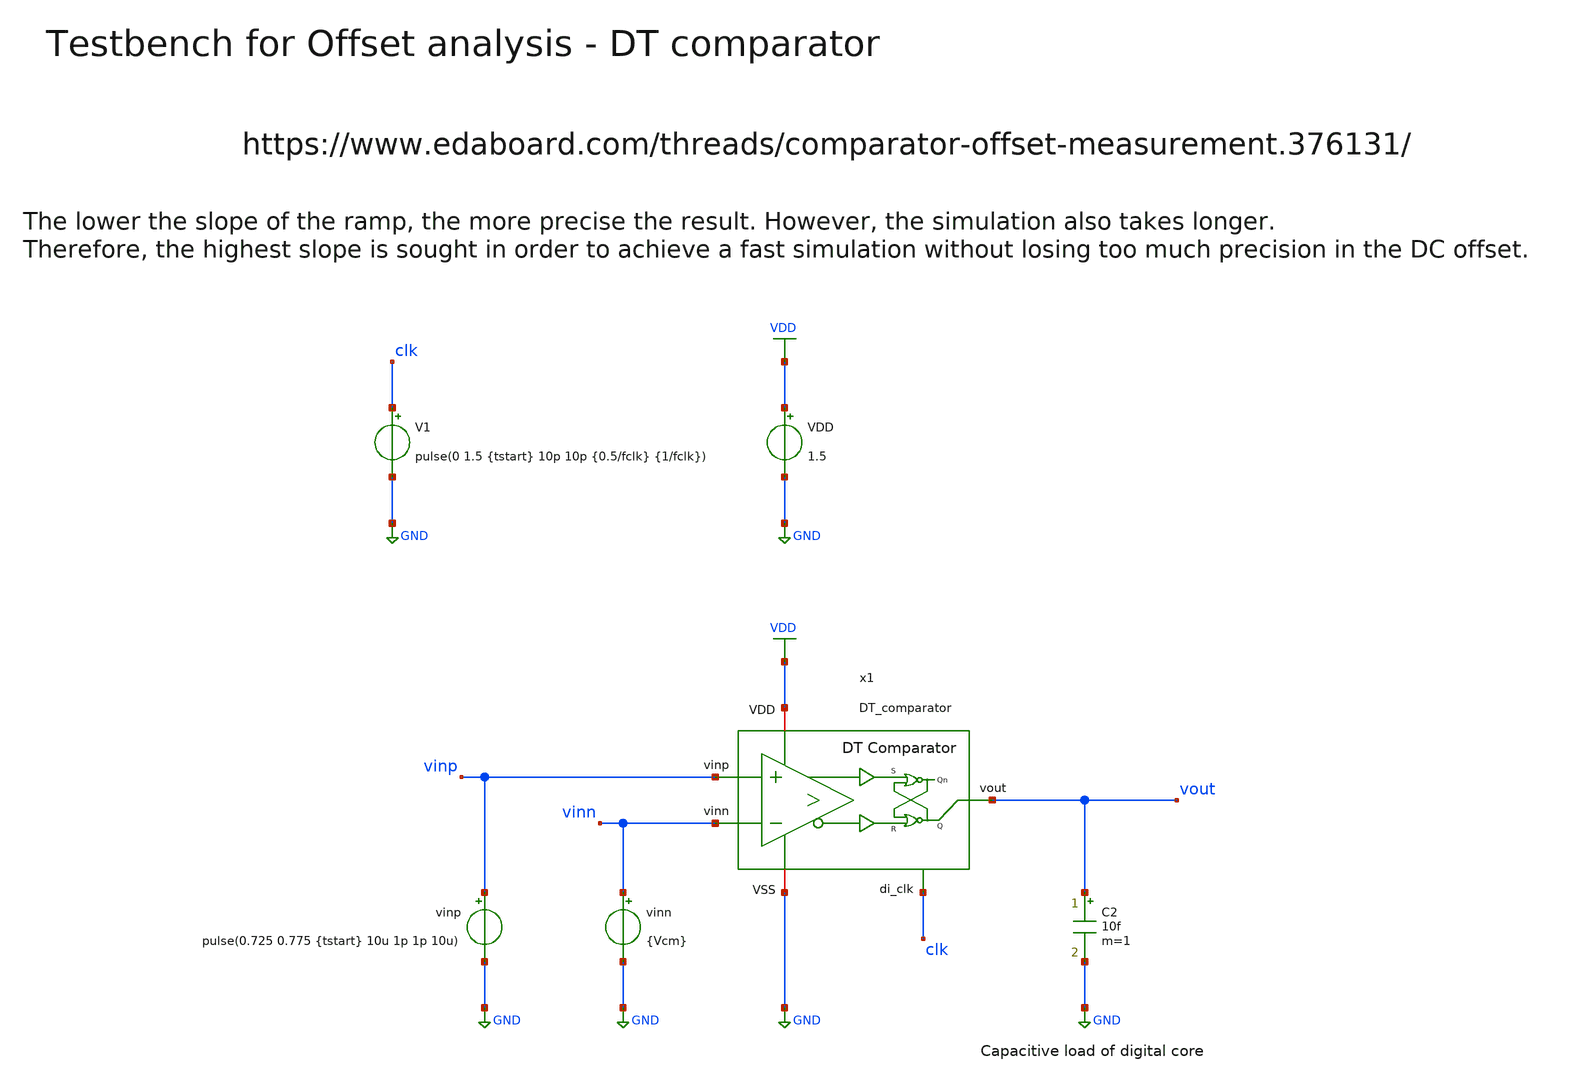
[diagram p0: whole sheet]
** sch_path: SG13G2_ATBS-ADC-main/xschem/comparator/discrete_time/testbenches/DT_comparator_tb_tran_offset.sch
**.subckt DT_comparator_tb_tran_offset
VDD VDD GND 1.5
V1 clk GND pulse(0 1.5 {tstart} 10p 10p {0.5/fclk} {1/fclk})
vinp vinp GND pulse(0.725 0.775 {tstart} 10u 1p 1p 10u)
vinn vinn GND {Vcm}
C2 vout GND 10f m=1
x1 VDD vinp vout vinn clk GND DT_comparator
**** begin user architecture code

.lib cornerMOSlv.lib mos_tt
.lib cornerMOShv.lib mos_tt
.lib cornerRES.lib res_typ



.param temp=27
.param fclk=8000000
.param tstart=2n
.param Vcm=0.75
.csparam fclk=fclk
.csparam tstart=tstart
.csparam Vcm=Vcm
.options klu method=gear reltol=1e-5 abstol=1e-12 gmin=1e-15
.ic v(vout) = 0
.control
* save all

* User Constants
let tstop = 10u
let tstep = 1/fclk

* Operating Point Analysis
op
remzerovec
write DT_comparator_tb_tran_offset.raw
set appendwrite

* Transient Analysis
tran $&tstep $&tstop
write DT_comparator_tb_tran_offset.raw

* Measure offset
let vout_limit = 0.9 * 1.5
meas tran tcross WHEN v(vout)=vout_limit CROSS=1
print tcross
meas tran vinp_voff FIND v(vinp) at=tcross CROSS=1
let voff = vinp_voff - Vcm
print voff

* Plotting
plot v(clk) v(vout) v(vinp) v(vinn)

* Writing Data
set wr_singlescale
set wr_vecnames
wrdata
+ /foss/designs/SG13G2_ATBS-ADC-main/python/plot_simulations/data/DT_comparator_tb_tran_offset.txt v(clk) v(vout) v(vinp) v(vinn)


*quit
.endc

**** end user architecture code
**.ends

* expanding   symbol:  comparator/discrete_time/DT_comparator.sym # of pins=6
** sym_path: SG13G2_ATBS-ADC-main/xschem/comparator/discrete_time/DT_comparator.sym
** sch_path: SG13G2_ATBS-ADC-main/xschem/comparator/discrete_time/DT_comparator.sch
.subckt DT_comparator VDD vinp vout vinn di_clk VSS
*.iopin VDD
*.opin vout
*.iopin VSS
*.ipin vinp
*.ipin vinn
*.ipin di_clk
x2 VDD voutp_comp voutp_buf VSS buffer_lv W_P_INV=1.0u L_P_INV=0.13u W_N_INV=1.0u L_N_INV=0.13u
x3 VDD voutn_comp voutn_buf VSS buffer_lv W_P_INV=1.0u L_P_INV=0.13u W_N_INV=1.0u L_N_INV=0.13u
x5 VDD di_clk net1 VSS inverter_lv W_P=1.0u L_P=0.13u W_N=1.0u L_N=0.13u
* noconn #net2
x4 VDD voutp_buf net2 VSS vout voutn_buf SR_latch W_P_SR=1.0u L_P_SR=0.13u W_N_SR=1.0u L_N_SR=0.13u
x1 net1 di_clk VDD voutp_comp vinp VSS voutn_comp vinn dynamic_biasing_comparator
.ends


* expanding   symbol:  buffer/buffer_lv.sym # of pins=4
** sym_path: SG13G2_ATBS-ADC-main/xschem/buffer/buffer_lv.sym
** sch_path: SG13G2_ATBS-ADC-main/xschem/buffer/buffer_lv.sch
.subckt buffer_lv VDD vin vout VSS  W_P_INV=3.0u L_P_INV=0.13u W_N_INV=1.0u L_N_INV=0.13u
*.ipin vin
*.iopin VDD
*.iopin VSS
*.opin vout
x1 VDD vin net1 VSS inverter_lv W_P=W_P_INV L_P=L_P_INV W_N=W_N_INV L_N=L_N_INV
x2 VDD net1 vout VSS inverter_lv W_P=W_P_INV L_P=L_P_INV W_N=W_N_INV L_N=L_N_INV
.ends


* expanding   symbol:  inverter/inverter_lv.sym # of pins=4
** sym_path: SG13G2_ATBS-ADC-main/xschem/inverter/inverter_lv.sym
** sch_path: SG13G2_ATBS-ADC-main/xschem/inverter/inverter_lv.sch
.subckt inverter_lv VDD vin vout VSS  W_P=3.0u L_P=0.13u W_N=1.0u L_N=0.13u
*.ipin vin
*.iopin VDD
*.iopin VSS
*.opin vout
XM1 vout vin VDD VDD sg13_lv_pmos w=W_P l=L_P ng=1 m=1 mm_ok=1
XM2 vout vin VSS VSS sg13_lv_nmos w=W_N l=L_N ng=1 m=1 mm_ok=1
.ends


* expanding   symbol:  comparator/SR_latch/SR_latch.sym # of pins=6
** sym_path: SG13G2_ATBS-ADC-main/xschem/comparator/SR_latch/SR_latch.sym
** sch_path: SG13G2_ATBS-ADC-main/xschem/comparator/SR_latch/SR_latch.sch
.subckt SR_latch VDD S Qn VSS Q R  W_P_SR=1.0u L_P_SR=0.13u W_N_SR=1.0u L_N_SR=0.13u
*.iopin VDD
*.opin Q
*.iopin VSS
*.ipin S
*.ipin R
*.opin Qn
x1 VDD Q R Qn VSS NOR_gate W_P=W_P_SR L_P=L_P_SR W_N=W_N_SR L_N=L_N_SR
x2 VDD Qn Q S VSS NOR_gate W_P=W_P_SR L_P=L_P_SR W_N=W_N_SR L_N=L_N_SR
.ends


* expanding   symbol:  comparator/discrete_time/Dynamic-biasing/dynamic_biasing_comparator.sym # of
*+ pins=8
** sym_path: SG13G2_ATBS-ADC-main/xschem/comparator/discrete_time/Dynamic-biasing/dynamic_biasing_comparator.sym
** sch_path: SG13G2_ATBS-ADC-main/xschem/comparator/discrete_time/Dynamic-biasing/dynamic_biasing_comparator.sch
.subckt dynamic_biasing_comparator di_clk_n di_clk VDD voutp vinp VSS voutn vinn
*.iopin VDD
*.opin voutp
*.opin voutn
*.ipin di_clk_n
*.iopin VSS
*.ipin vinp
*.ipin vinn
*.ipin di_clk
XM3a vs di_clk vctail VSS sg13_lv_nmos w=1.0u l=0.13u ng=1 m=1 mm_ok=1
XM12 voutp di_clk_n VSS VSS sg13_lv_nmos w=1.0u l=0.13u ng=1 m=1 mm_ok=1
XM8 net1 voutn VDD VDD sg13_lv_pmos w=2.0u l=0.13u ng=2 m=1 mm_ok=1
XM10 voutp voutn VSS VSS sg13_lv_nmos w=1.0u l=0.13u ng=1 m=1 mm_ok=1
XM11 voutn voutp VSS VSS sg13_lv_nmos w=1.0u l=0.13u ng=1 m=1 mm_ok=1
XM13 voutn di_clk_n VSS VSS sg13_lv_nmos w=1.0u l=0.13u ng=1 m=1 mm_ok=1
CPn vcpn VSS 300f m=1
CPp vcpp VSS 300f m=1
XM9 net2 voutp VDD VDD sg13_lv_pmos w=2.0u l=0.13u ng=2 m=1 mm_ok=1
XM6 voutp vcpn net1 VDD sg13_lv_pmos w=2.0u l=0.13u ng=2 m=1 mm_ok=1
XM7 voutn vcpp net2 VDD sg13_lv_pmos w=2.0u l=0.13u ng=2 m=1 mm_ok=1
CTAIL vctail VSS 600f m=1
XM3b vctail di_clk_n VSS VSS sg13_lv_nmos w=1.0u l=0.13u ng=1 m=1 mm_ok=1
XM1 vcpn vinp vs VSS sg13_lv_nmos w=1.0u l=0.13u ng=1 m=1 mm_ok=1
XM2 vcpp vinn vs VSS sg13_lv_nmos w=1.0u l=0.13u ng=1 m=1 mm_ok=1
XM4 vcpn di_clk VDD VDD sg13_lv_pmos w=1.0u l=0.13u ng=1 m=1 mm_ok=1
XM5 vcpp di_clk VDD VDD sg13_lv_pmos w=1.0u l=0.13u ng=1 m=1 mm_ok=1
.ends


* expanding   symbol:  comparator/NOR_gate/NOR_gate.sym # of pins=5
** sym_path: SG13G2_ATBS-ADC-main/xschem/comparator/NOR_gate/NOR_gate.sym
** sch_path: SG13G2_ATBS-ADC-main/xschem/comparator/NOR_gate/NOR_gate.sch
.subckt NOR_gate VDD C A B VSS  W_P=1.0u L_P=0.13u W_N=0.5u L_N=0.13u
*.iopin VDD
*.opin C
*.iopin VSS
*.ipin A
*.ipin B
XM1 C A VSS VSS sg13_lv_nmos w=W_N l=L_N ng=1 m=1 mm_ok=1
XM2 C B VSS VSS sg13_lv_nmos w=W_N l=L_N ng=1 m=1 mm_ok=1
XM3 C B net1 VDD sg13_lv_pmos w=W_P l=L_P ng=1 m=1 mm_ok=1
XM4 net1 A VDD VDD sg13_lv_pmos w=W_P l=L_P ng=1 m=1 mm_ok=1
XM5 C A net2 VDD sg13_lv_pmos w=W_P l=L_P ng=1 m=1 mm_ok=1
XM6 net2 B VDD VDD sg13_lv_pmos w=W_P l=L_P ng=1 m=1 mm_ok=1
.ends

.GLOBAL GND
.GLOBAL VDD
.end
